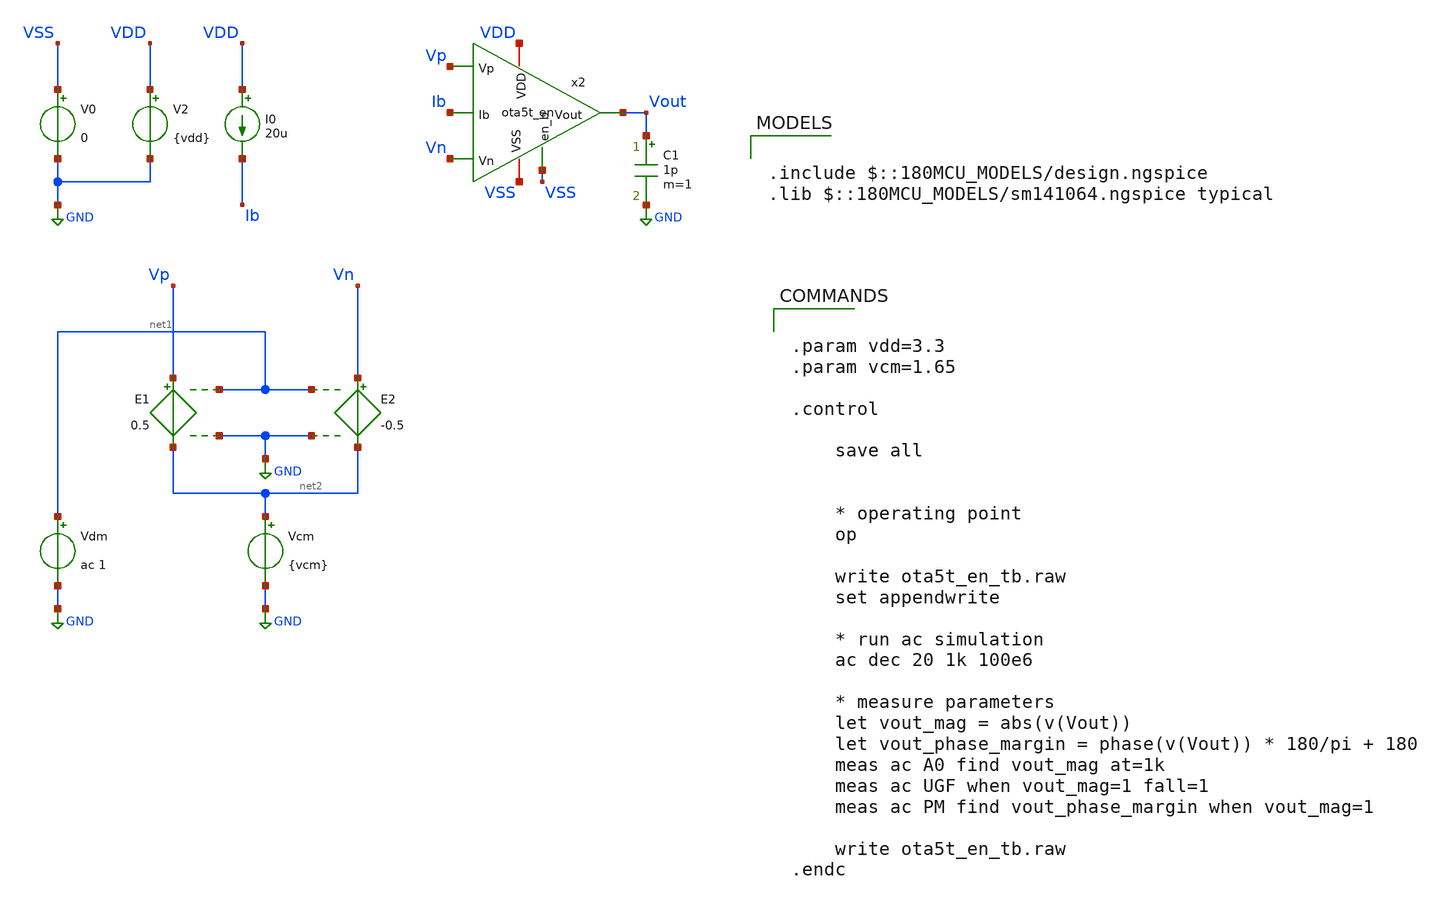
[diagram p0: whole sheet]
** sch_path: Analog/schematics/1_readout/tia/old/ota5t_en_tb.sch
**.subckt ota5t_en_tb
I0 VDD Ib 20u
C1 Vout GND 1p m=1
V0 VSS GND 0
V2 VDD GND {vdd}
E1 Vp net2 net1 GND 0.5
E2 Vn net2 net1 GND -0.5
Vdm net1 GND ac 1
Vcm net2 GND {vcm}
x2 Vp Vn Vout VDD VSS Ib VSS ota5t_en
**** begin user architecture code


.param vdd=3.3
.param vcm=1.65

.control

    save all


    * operating point
    op

    write ota5t_en_tb.raw
    set appendwrite

    * run ac simulation
    ac dec 20 1k 100e6

    * measure parameters
    let vout_mag = abs(v(Vout))
    let vout_phase_margin = phase(v(Vout)) * 180/pi + 180
    meas ac A0 find vout_mag at=1k
    meas ac UGF when vout_mag=1 fall=1
    meas ac PM find vout_phase_margin when vout_mag=1

    write ota5t_en_tb.raw
.endc



.include $::180MCU_MODELS/design.ngspice
.lib $::180MCU_MODELS/sm141064.ngspice typical

**** end user architecture code
**.ends
.GLOBAL GND
.end
